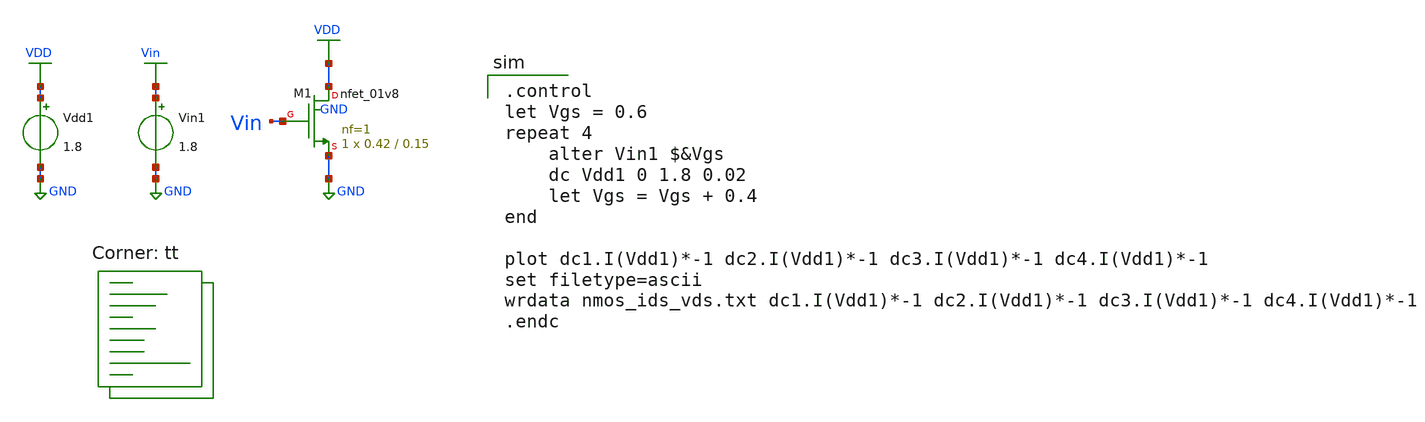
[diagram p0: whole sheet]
** sch_path: tutorial-1/source/q1b.sch
**.subckt q1b
Vdd1 VDD GND 1.8
Vin1 Vin GND 1.8
XM1 VDD Vin GND GND sky130_fd_pr__nfet_01v8 L=0.15 W=0.42 nf=1 ad='int((nf+1)/2) * W/nf * 0.29' as='int((nf+2)/2) * W/nf * 0.29'
+ pd='2*int((nf+1)/2) * (W/nf + 0.29)' ps='2*int((nf+2)/2) * (W/nf + 0.29)' nrd='0.29 / W' nrs='0.29 / W'
+ sa=0 sb=0 sd=0 mult=1 m=1
**** begin user architecture code
.lib $::SKYWATER_MODELS/sky130.lib.spice tt

.control
let Vgs = 0.6
repeat 4
    alter Vin1 $&Vgs
    dc Vdd1 0 1.8 0.02
    let Vgs = Vgs + 0.4
end

plot dc1.I(Vdd1)*-1 dc2.I(Vdd1)*-1 dc3.I(Vdd1)*-1 dc4.I(Vdd1)*-1
set filetype=ascii
wrdata nmos_ids_vds.txt dc1.I(Vdd1)*-1 dc2.I(Vdd1)*-1 dc3.I(Vdd1)*-1 dc4.I(Vdd1)*-1
.endc

**** end user architecture code
**.ends
.GLOBAL VDD
.GLOBAL GND
.GLOBAL Vin
.end
